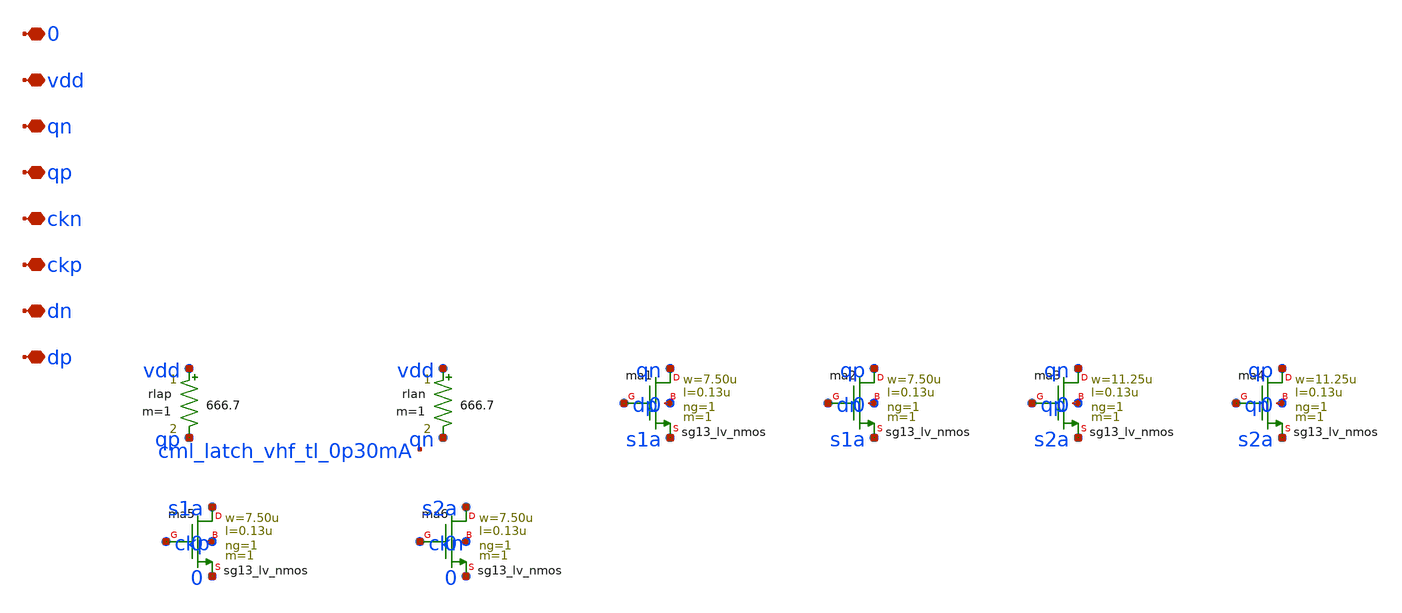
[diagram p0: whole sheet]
** sch_path: analog/lo/sch/cml_latch_vhf_tl.sch
**.subckt cml_latch_vhf_tl dp dn ckp ckn qp qn vdd 0
*.iopin dp
*.iopin dn
*.iopin ckp
*.iopin ckn
*.iopin qp
*.iopin qn
*.iopin vdd
*.iopin 0
rlap vdd qp 666.7 m=1
rlan vdd qn 666.7 m=1
Xma1 qn dp s1a 0 sg13_lv_nmos w=7.50u l=0.13u ng=1 m=1 mm_ok=1
Xma2 qp dn s1a 0 sg13_lv_nmos w=7.50u l=0.13u ng=1 m=1 mm_ok=1
Xma3 qn qp s2a 0 sg13_lv_nmos w=11.25u l=0.13u ng=1 m=1 mm_ok=1
Xma4 qp qn s2a 0 sg13_lv_nmos w=11.25u l=0.13u ng=1 m=1 mm_ok=1
Xma5 s1a ckp 0 0 sg13_lv_nmos w=7.50u l=0.13u ng=1 m=1 mm_ok=1
Xma6 s2a ckn 0 0 sg13_lv_nmos w=7.50u l=0.13u ng=1 m=1 mm_ok=1
**.ends
.end
